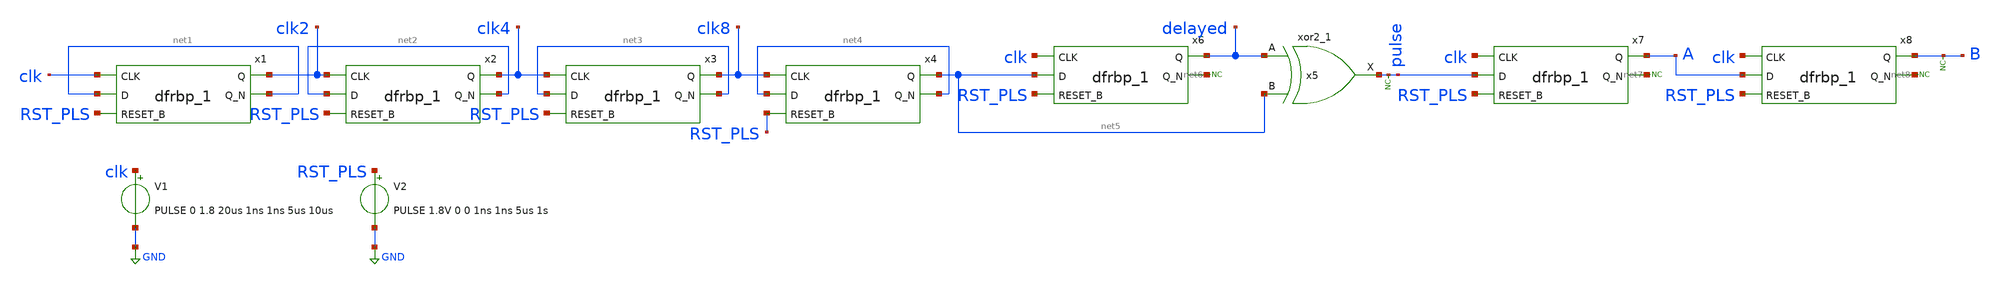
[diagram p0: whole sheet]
** sch_path: pulse_generator.sch
**.subckt pulse_generator
x1 clk net1 RST_PLS GND GND VCC VCC clk2 net1 sky130_fd_sc_hd__dfrbp_1
x2 clk2 net2 RST_PLS GND GND VCC VCC clk4 net2 sky130_fd_sc_hd__dfrbp_1
x3 clk4 net3 RST_PLS GND GND VCC VCC clk8 net3 sky130_fd_sc_hd__dfrbp_1
x4 clk8 net4 RST_PLS GND GND VCC VCC net5 net4 sky130_fd_sc_hd__dfrbp_1
x5 delayed net5 GND GND VCC VCC pulse sky130_fd_sc_hd__xor2_1
V1 clk GND PULSE 0 1.8 20us 1ns 1ns 5us 10us
V2 RST_PLS GND PULSE 1.8V 0 0 1ns 1ns 5us 1s
* noconn pulse
x6 clk net5 RST_PLS GND GND VCC VCC delayed net6 sky130_fd_sc_hd__dfrbp_1
* noconn #net6
x7 clk pulse RST_PLS GND GND VCC VCC A net7 sky130_fd_sc_hd__dfrbp_1
* noconn #net7
x8 clk A RST_PLS GND GND VCC VCC B net8 sky130_fd_sc_hd__dfrbp_1
* noconn #net8
* noconn B
**** begin user architecture code
 .lib $::SKYWATER_MODELS/sky130.lib.spice tt
.include $::SKYWATER_STDCELLS/sky130_fd_sc_hd.spice



.options acct list
.temp 25
vvcc VCC 0 dc 1.8
*vvss GND 0 0
.control
tran 0.1u 150u
* plot a b+2 clk+4 reset_b+6 x+8 y+10 q+12 qlatch+14
plot RST_PLS-2 clk clk2+2 clk4+4 clk8+6 pulse+8 delayed+10
write pulse_generator.raw
.endc


**** end user architecture code
**.ends
.GLOBAL GND
.end
